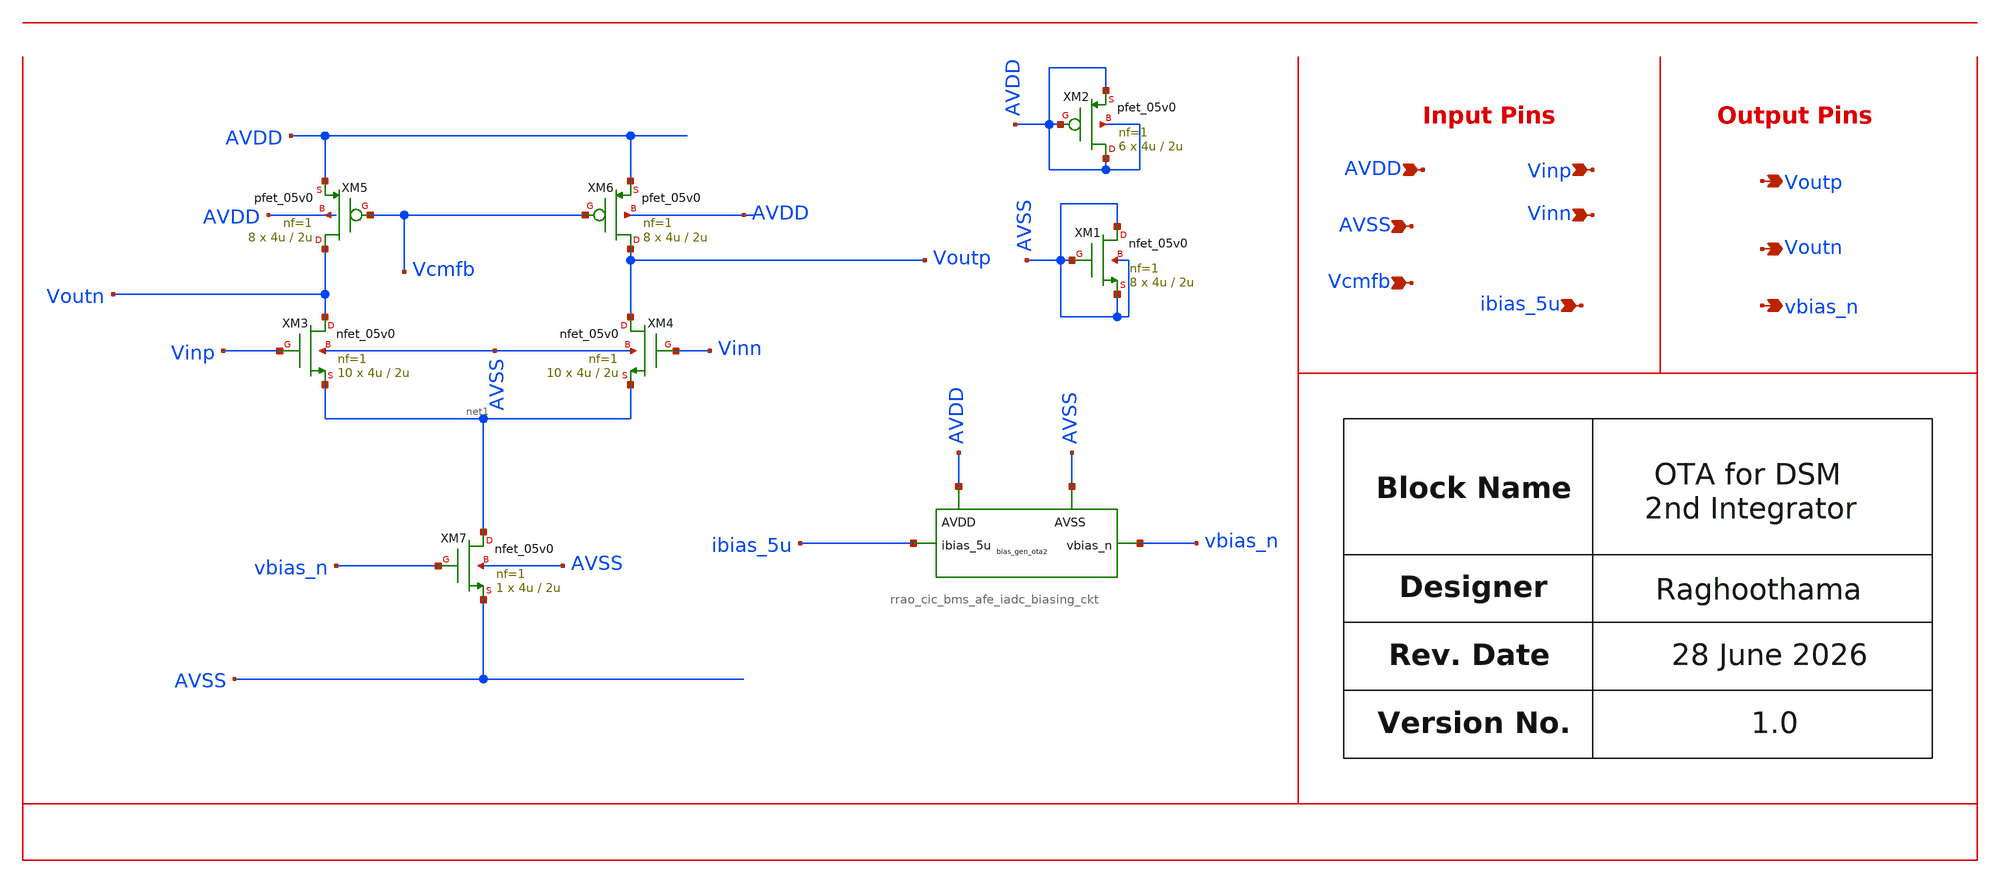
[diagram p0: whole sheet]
** sch_path: design/schematics/ADC/Adder/OTA/rrao_cic_bms_afe_iadc_second_int_ota.sch
**.subckt rrao_cic_bms_afe_iadc_second_int_ota Vinp Voutn Voutp Vinn ibias_5u AVDD AVSS Vcmfb
*+ vbias_n
*.ipin Vinp
*.opin Voutn
*.opin Voutp
*.ipin Vinn
*.ipin ibias_5u
*.ipin AVDD
*.ipin AVSS
*.ipin Vcmfb
*.opin vbias_n
XM3 Voutn Vinp net1 AVSS nfet_05v0 L=2u W=4u nf=1 ad='int((nf+1)/2) * W/nf * 0.18u' as='int((nf+2)/2) * W/nf * 0.18u'
+ pd='2*int((nf+1)/2) * (W/nf + 0.18u)' ps='2*int((nf+2)/2) * (W/nf + 0.18u)' nrd='0.18u / W' nrs='0.18u / W'
+ sa=0 sb=0 sd=0 m=10
XM4 Voutp Vinn net1 AVSS nfet_05v0 L=2u W=4u nf=1 ad='int((nf+1)/2) * W/nf * 0.18u' as='int((nf+2)/2) * W/nf * 0.18u'
+ pd='2*int((nf+1)/2) * (W/nf + 0.18u)' ps='2*int((nf+2)/2) * (W/nf + 0.18u)' nrd='0.18u / W' nrs='0.18u / W'
+ sa=0 sb=0 sd=0 m=10
XM5 Voutn Vcmfb AVDD AVDD pfet_05v0 L=2u W=4u nf=1 ad='int((nf+1)/2) * W/nf * 0.18u' as='int((nf+2)/2) * W/nf * 0.18u'
+ pd='2*int((nf+1)/2) * (W/nf + 0.18u)' ps='2*int((nf+2)/2) * (W/nf + 0.18u)' nrd='0.18u / W' nrs='0.18u / W'
+ sa=0 sb=0 sd=0 m=8
XM6 Voutp Vcmfb AVDD AVDD pfet_05v0 L=2u W=4u nf=1 ad='int((nf+1)/2) * W/nf * 0.18u' as='int((nf+2)/2) * W/nf * 0.18u'
+ pd='2*int((nf+1)/2) * (W/nf + 0.18u)' ps='2*int((nf+2)/2) * (W/nf + 0.18u)' nrd='0.18u / W' nrs='0.18u / W'
+ sa=0 sb=0 sd=0 m=8
XM7 net1 vbias_n AVSS AVSS nfet_05v0 L=2u W=4u nf=1 ad='int((nf+1)/2) * W/nf * 0.18u' as='int((nf+2)/2) * W/nf * 0.18u'
+ pd='2*int((nf+1)/2) * (W/nf + 0.18u)' ps='2*int((nf+2)/2) * (W/nf + 0.18u)' nrd='0.18u / W' nrs='0.18u / W'
+ sa=0 sb=0 sd=0 m=1
x1 AVDD AVSS ibias_5u vbias_n rrao_cic_bms_afe_iadc_biasing_ckt
XM1 AVSS AVSS AVSS AVSS nfet_05v0 L=2u W=4u nf=1 ad='int((nf+1)/2) * W/nf * 0.18u' as='int((nf+2)/2) * W/nf * 0.18u'
+ pd='2*int((nf+1)/2) * (W/nf + 0.18u)' ps='2*int((nf+2)/2) * (W/nf + 0.18u)' nrd='0.18u / W' nrs='0.18u / W'
+ sa=0 sb=0 sd=0 m=8
XM2 AVDD AVDD AVDD AVDD pfet_05v0 L=2u W=4u nf=1 ad='int((nf+1)/2) * W/nf * 0.18u' as='int((nf+2)/2) * W/nf * 0.18u'
+ pd='2*int((nf+1)/2) * (W/nf + 0.18u)' ps='2*int((nf+2)/2) * (W/nf + 0.18u)' nrd='0.18u / W' nrs='0.18u / W'
+ sa=0 sb=0 sd=0 m=6
**.ends
.end
